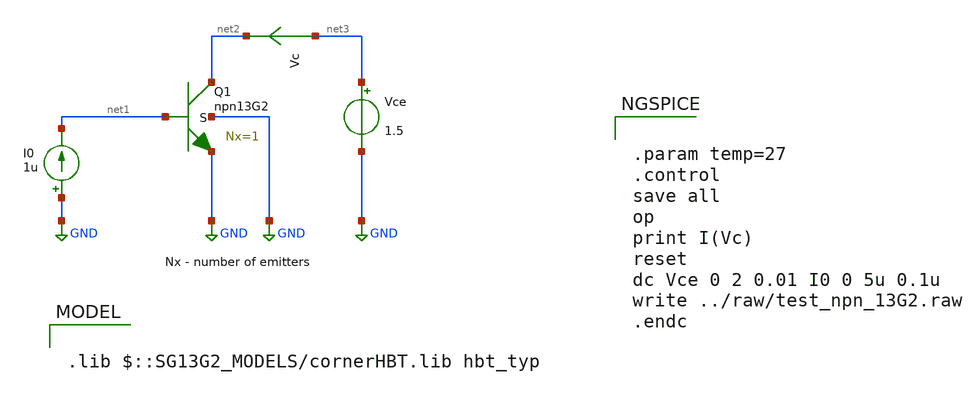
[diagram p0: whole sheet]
** sch_path: ihp-sg13g2/libs.tech/xschem/sg13g2_tests/dc_hbt_13g2.sch
* Copyright 2023 IHP PDK Authors
**.subckt dc_hbt_13g2
Vce net3 GND 1.5
XQ1 net2 net1 GND GND npn13G2 Nx=1 mm_ok=1
I0 GND net1 1u
Vc net3 net2 0
.save i(vc)
**** begin user architecture code

.lib $::SG13G2_MODELS/cornerHBT.lib hbt_typ



.param temp=27
.control
save all
op
print I(Vc)
reset
dc Vce 0 2 0.01 I0 0 5u 0.1u
write ../raw/test_npn_13G2.raw
.endc


**** end user architecture code
**.ends
.GLOBAL GND
.end
